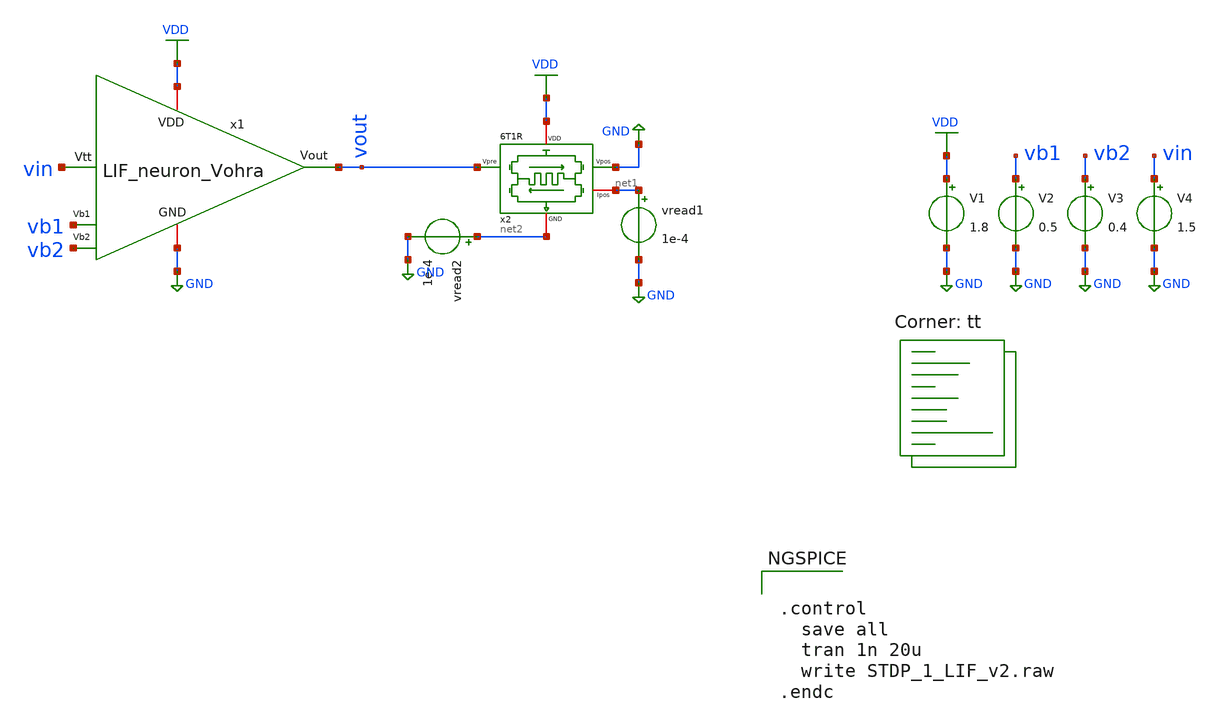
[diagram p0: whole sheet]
** sch_path: STDP/STDP_1_LIF_v2.sch
**.subckt STDP_1_LIF_v2
x1 VDD vout vb1 vin GND vb2 LIF_neuron_Vohra
V1 VDD GND 1.8
V4 vin GND 1.5
V2 vb1 GND 0.5
V3 vb2 GND 0.4
x2 VDD net1 vout GND net2 6T1R
vread1 net1 GND 1e-4
vread2 net2 GND 1e-4
**** begin user architecture code
.lib $::SKYWATER_MODELS/sky130.lib.spice tt

** opencircuitdesign pdks install
.inc $::SKYWATER_MODELS/rram_v0.spice



.control
  save all
  tran 1n 20u
  write STDP_1_LIF_v2.raw
.endc


**** end user architecture code
**.ends

* expanding   symbol:  /home/ricardoatt/RATT_repos/Proyectos_xschem/LIF_neuron/LIF_neuron_Vohra.sym
*+ # of pins=6
** sym_path: LIF_neuron/LIF_neuron_Vohra.sym
** sch_path: LIF_neuron/LIF_neuron_Vohra.sch
.subckt LIF_neuron_Vohra VDD Vout Vb1 Vtt GND Vb2
*.ipin Vtt
*.iopin GND
*.ipin Vb1
*.ipin Vb2
*.iopin VDD
*.opin Vout
XM1 net4 Vtt GND GND sky130_fd_pr__nfet_01v8 L=1 W=0.6 nf=1 ad='int((nf+1)/2) * W/nf * 0.29' as='int((nf+2)/2) * W/nf * 0.29'
+ pd='2*int((nf+1)/2) * (W/nf + 0.29)' ps='2*int((nf+2)/2) * (W/nf + 0.29)' nrd='0.29 / W' nrs='0.29 / W'
+ sa=0 sb=0 sd=0 mult=1 m=1
XM3 net4 net4 VDD VDD sky130_fd_pr__pfet_01v8 L=1 W=0.6 nf=1 ad='int((nf+1)/2) * W/nf * 0.29' as='int((nf+2)/2) * W/nf * 0.29'
+ pd='2*int((nf+1)/2) * (W/nf + 0.29)' ps='2*int((nf+2)/2) * (W/nf + 0.29)' nrd='0.29 / W' nrs='0.29 / W'
+ sa=0 sb=0 sd=0 mult=1 m=1
XM13 net3 Vb1 GND GND sky130_fd_pr__nfet_01v8 L=0.5 W=5 nf=1 ad='int((nf+1)/2) * W/nf * 0.29' as='int((nf+2)/2) * W/nf * 0.29'
+ pd='2*int((nf+1)/2) * (W/nf + 0.29)' ps='2*int((nf+2)/2) * (W/nf + 0.29)' nrd='0.29 / W' nrs='0.29 / W'
+ sa=0 sb=0 sd=0 mult=1 m=1
XM12 net1 net2 net3 GND sky130_fd_pr__nfet_01v8 L=1 W=1 nf=1 ad='int((nf+1)/2) * W/nf * 0.29' as='int((nf+2)/2) * W/nf * 0.29'
+ pd='2*int((nf+1)/2) * (W/nf + 0.29)' ps='2*int((nf+2)/2) * (W/nf + 0.29)' nrd='0.29 / W' nrs='0.29 / W'
+ sa=0 sb=0 sd=0 mult=1 m=1
XM11 net1 net2 VDD VDD sky130_fd_pr__pfet_01v8 L=1 W=1 nf=1 ad='int((nf+1)/2) * W/nf * 0.29' as='int((nf+2)/2) * W/nf * 0.29'
+ pd='2*int((nf+1)/2) * (W/nf + 0.29)' ps='2*int((nf+2)/2) * (W/nf + 0.29)' nrd='0.29 / W' nrs='0.29 / W'
+ sa=0 sb=0 sd=0 mult=1 m=1
XC1 net1 GND sky130_fd_pr__cap_mim_m3_1 W=21 L=1 MF=1 m=1
XM14 net5 net1 GND GND sky130_fd_pr__nfet_01v8 L=1 W=1 nf=1 ad='int((nf+1)/2) * W/nf * 0.29' as='int((nf+2)/2) * W/nf * 0.29'
+ pd='2*int((nf+1)/2) * (W/nf + 0.29)' ps='2*int((nf+2)/2) * (W/nf + 0.29)' nrd='0.29 / W' nrs='0.29 / W'
+ sa=0 sb=0 sd=0 mult=1 m=1
XM4 net5 net4 VDD VDD sky130_fd_pr__pfet_01v8 L=1 W=1 nf=1 ad='int((nf+1)/2) * W/nf * 0.29' as='int((nf+2)/2) * W/nf * 0.29'
+ pd='2*int((nf+1)/2) * (W/nf + 0.29)' ps='2*int((nf+2)/2) * (W/nf + 0.29)' nrd='0.29 / W' nrs='0.29 / W'
+ sa=0 sb=0 sd=0 mult=1 m=1
XC2 net5 GND sky130_fd_pr__cap_mim_m3_1 W=10 L=1 MF=50 m=50
XM5 net5 Vb2 GND GND sky130_fd_pr__nfet_01v8 L=1 W=2 nf=1 ad='int((nf+1)/2) * W/nf * 0.29' as='int((nf+2)/2) * W/nf * 0.29'
+ pd='2*int((nf+1)/2) * (W/nf + 0.29)' ps='2*int((nf+2)/2) * (W/nf + 0.29)' nrd='0.29 / W' nrs='0.29 / W'
+ sa=0 sb=0 sd=0 mult=1 m=1
XM6 net6 Vout GND GND sky130_fd_pr__nfet_01v8 L=1 W=1 nf=1 ad='int((nf+1)/2) * W/nf * 0.29' as='int((nf+2)/2) * W/nf * 0.29'
+ pd='2*int((nf+1)/2) * (W/nf + 0.29)' ps='2*int((nf+2)/2) * (W/nf + 0.29)' nrd='0.29 / W' nrs='0.29 / W'
+ sa=0 sb=0 sd=0 mult=1 m=1
XM7 net2 net5 net6 GND sky130_fd_pr__nfet_01v8 L=1 W=1 nf=1 ad='int((nf+1)/2) * W/nf * 0.29' as='int((nf+2)/2) * W/nf * 0.29'
+ pd='2*int((nf+1)/2) * (W/nf + 0.29)' ps='2*int((nf+2)/2) * (W/nf + 0.29)' nrd='0.29 / W' nrs='0.29 / W'
+ sa=0 sb=0 sd=0 mult=1 m=1
XM8 net2 net5 VDD VDD sky130_fd_pr__pfet_01v8 L=1 W=1 nf=1 ad='int((nf+1)/2) * W/nf * 0.29' as='int((nf+2)/2) * W/nf * 0.29'
+ pd='2*int((nf+1)/2) * (W/nf + 0.29)' ps='2*int((nf+2)/2) * (W/nf + 0.29)' nrd='0.29 / W' nrs='0.29 / W'
+ sa=0 sb=0 sd=0 mult=1 m=1
XM9 Vout net2 net6 GND sky130_fd_pr__nfet_01v8 L=1 W=1 nf=1 ad='int((nf+1)/2) * W/nf * 0.29' as='int((nf+2)/2) * W/nf * 0.29'
+ pd='2*int((nf+1)/2) * (W/nf + 0.29)' ps='2*int((nf+2)/2) * (W/nf + 0.29)' nrd='0.29 / W' nrs='0.29 / W'
+ sa=0 sb=0 sd=0 mult=1 m=1
XM10 Vout net2 VDD VDD sky130_fd_pr__pfet_01v8 L=1 W=5 nf=1 ad='int((nf+1)/2) * W/nf * 0.29' as='int((nf+2)/2) * W/nf * 0.29'
+ pd='2*int((nf+1)/2) * (W/nf + 0.29)' ps='2*int((nf+2)/2) * (W/nf + 0.29)' nrd='0.29 / W' nrs='0.29 / W'
+ sa=0 sb=0 sd=0 mult=1 m=1
.ends


* expanding   symbol:  /home/ricardoatt/RATT_repos/Proyectos_xschem/synapse/6T1R.sym # of pins=5
** sym_path: synapse/6T1R.sym
** sch_path: synapse/6T1R.sch
.subckt 6T1R VDD Ipos Vpre Vpos GND
*.ipin Vpre
*.ipin Vpos
*.iopin GND
*.iopin Ipos
*.iopin VDD
XM1 BE Vpre vipre GND sky130_fd_pr__nfet_01v8 L=0.15 W=15 nf=1 ad='int((nf+1)/2) * W/nf * 0.29' as='int((nf+2)/2) * W/nf * 0.29'
+ pd='2*int((nf+1)/2) * (W/nf + 0.29)' ps='2*int((nf+2)/2) * (W/nf + 0.29)' nrd='0.29 / W' nrs='0.29 / W'
+ sa=0 sb=0 sd=0 mult=1 m=1
XR1 TE BE rram_v0
XM3 TE Vpos vipre GND sky130_fd_pr__nfet_01v8 L=0.15 W=15 nf=1 ad='int((nf+1)/2) * W/nf * 0.29' as='int((nf+2)/2) * W/nf * 0.29'
+ pd='2*int((nf+1)/2) * (W/nf + 0.29)' ps='2*int((nf+2)/2) * (W/nf + 0.29)' nrd='0.29 / W' nrs='0.29 / W'
+ sa=0 sb=0 sd=0 mult=1 m=1
XM6 Ipos vipre VDD VDD sky130_fd_pr__pfet_01v8 L=0.15 W=20 nf=1 ad='int((nf+1)/2) * W/nf * 0.29' as='int((nf+2)/2) * W/nf * 0.29'
+ pd='2*int((nf+1)/2) * (W/nf + 0.29)' ps='2*int((nf+2)/2) * (W/nf + 0.29)' nrd='0.29 / W' nrs='0.29 / W'
+ sa=0 sb=0 sd=0 mult=1 m=1
XM5 vipre vipre VDD VDD sky130_fd_pr__pfet_01v8 L=0.15 W=20 nf=1 ad='int((nf+1)/2) * W/nf * 0.29' as='int((nf+2)/2) * W/nf * 0.29'
+ pd='2*int((nf+1)/2) * (W/nf + 0.29)' ps='2*int((nf+2)/2) * (W/nf + 0.29)' nrd='0.29 / W' nrs='0.29 / W'
+ sa=0 sb=0 sd=0 mult=1 m=1
XM2 GND Vpos BE GND sky130_fd_pr__nfet_01v8 L=0.15 W=15 nf=1 ad='int((nf+1)/2) * W/nf * 0.29' as='int((nf+2)/2) * W/nf * 0.29'
+ pd='2*int((nf+1)/2) * (W/nf + 0.29)' ps='2*int((nf+2)/2) * (W/nf + 0.29)' nrd='0.29 / W' nrs='0.29 / W'
+ sa=0 sb=0 sd=0 mult=1 m=1
XM4 GND Vpre TE GND sky130_fd_pr__nfet_01v8 L=0.15 W=15 nf=1 ad='int((nf+1)/2) * W/nf * 0.29' as='int((nf+2)/2) * W/nf * 0.29'
+ pd='2*int((nf+1)/2) * (W/nf + 0.29)' ps='2*int((nf+2)/2) * (W/nf + 0.29)' nrd='0.29 / W' nrs='0.29 / W'
+ sa=0 sb=0 sd=0 mult=1 m=1
.ends

.GLOBAL GND
.GLOBAL VDD
.end
